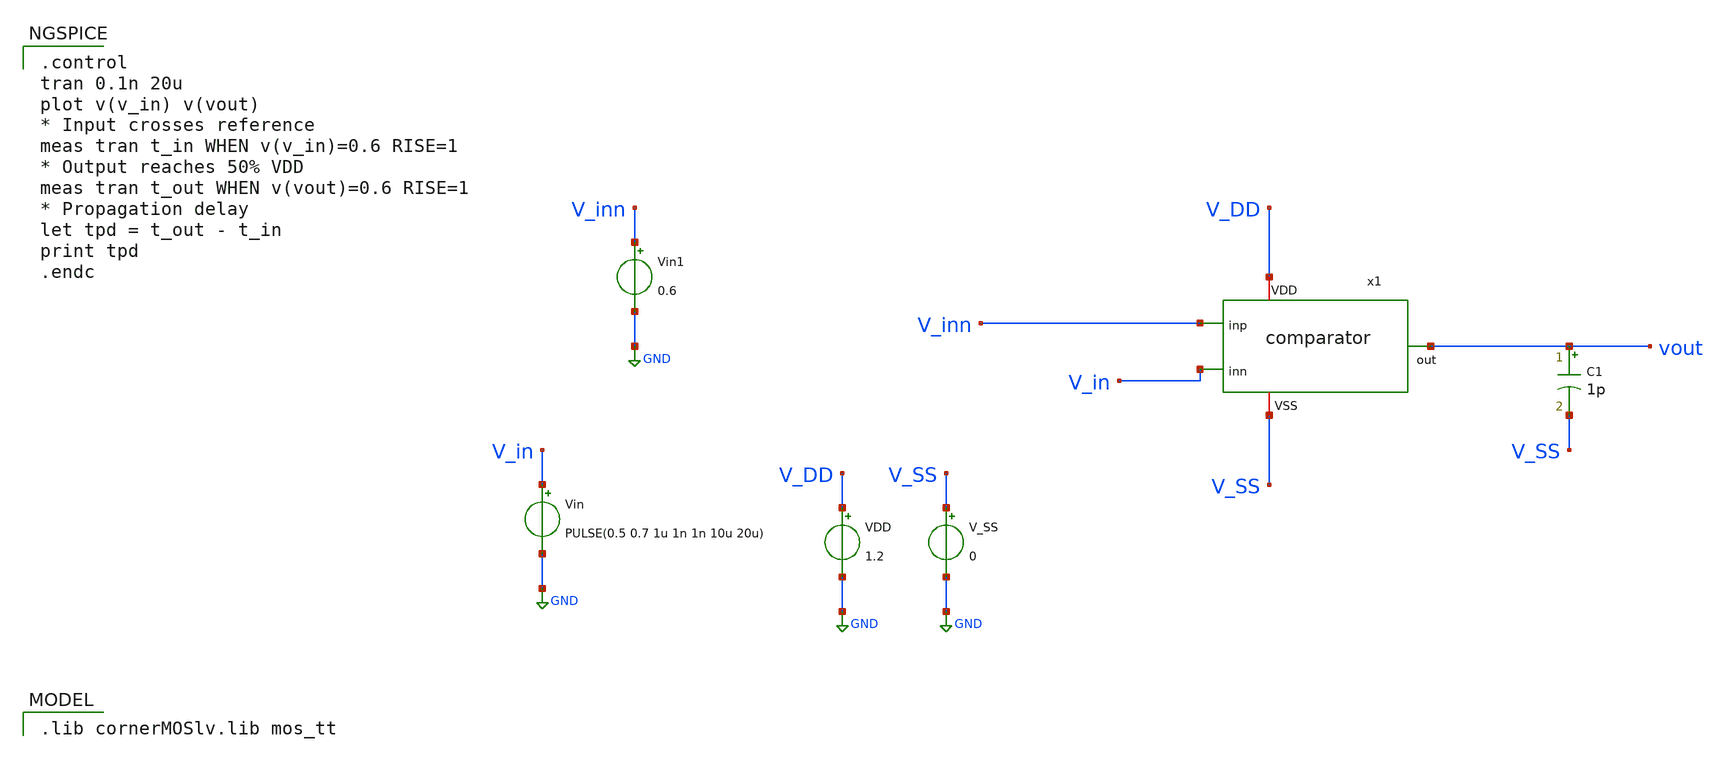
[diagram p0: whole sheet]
** sch_path: xschem/comparator_tb_tran.sch
**.subckt comparator_tb_tran
C1 vout V_SS 1p m=1
Vin V_in GND PULSE(0.5 0.7 1u 1n 1n 10u 20u)
VDD V_DD GND 1.2
V_SS V_SS GND 0
x1 V_DD vout V_in V_inn V_SS comparator
Vin1 V_inn GND 0.6
**** begin user architecture code
 .lib cornerMOSlv.lib mos_tt


.control
tran 0.1n 20u
plot v(v_in) v(vout)
* Input crosses reference
meas tran t_in WHEN v(v_in)=0.6 RISE=1
* Output reaches 50% VDD
meas tran t_out WHEN v(vout)=0.6 RISE=1
* Propagation delay
let tpd = t_out - t_in
print tpd
.endc


**** end user architecture code
**.ends

* expanding   symbol:  comparator.sym # of pins=5
** sym_path: xschem/comparator.sym
** sch_path: xschem/comparator.sch
.subckt comparator VDD out inn inp VSS
*.ipin inp
*.ipin inn
*.iopin VDD
*.iopin VSS
*.opin out
XM4 net2 net1 VDD VDD sg13_lv_pmos w=1.5u l=5u ng=1 m=1 mm_ok=1
XM3 net1 net1 VDD VDD sg13_lv_pmos w=1.5u l=5u ng=1 m=1 mm_ok=1
XM1 net1 inp net3 VSS sg13_lv_nmos w=1.5u l=5u ng=1 m=1 mm_ok=1
XM2 net2 inn net3 VSS sg13_lv_nmos w=1.5u l=5u ng=1 m=1 mm_ok=1
XM7 net4 net4 VDD VDD sg13_lv_pmos w=1.5u l=5u ng=1 m=1 mm_ok=1
XM8 out net2 VDD VDD sg13_lv_pmos w=1.5u l=5u ng=1 m=1 mm_ok=1
XM6 net4 net4 VSS VSS sg13_lv_nmos w=2.5u l=5u ng=1 m=1 mm_ok=1
XM5 net3 net4 VSS VSS sg13_lv_nmos w=1.5u l=5u ng=1 m=1 mm_ok=1
XM9 out net4 VSS VSS sg13_lv_nmos w=1.5u l=5u ng=1 m=1 mm_ok=1
.ends

.GLOBAL GND
.end
